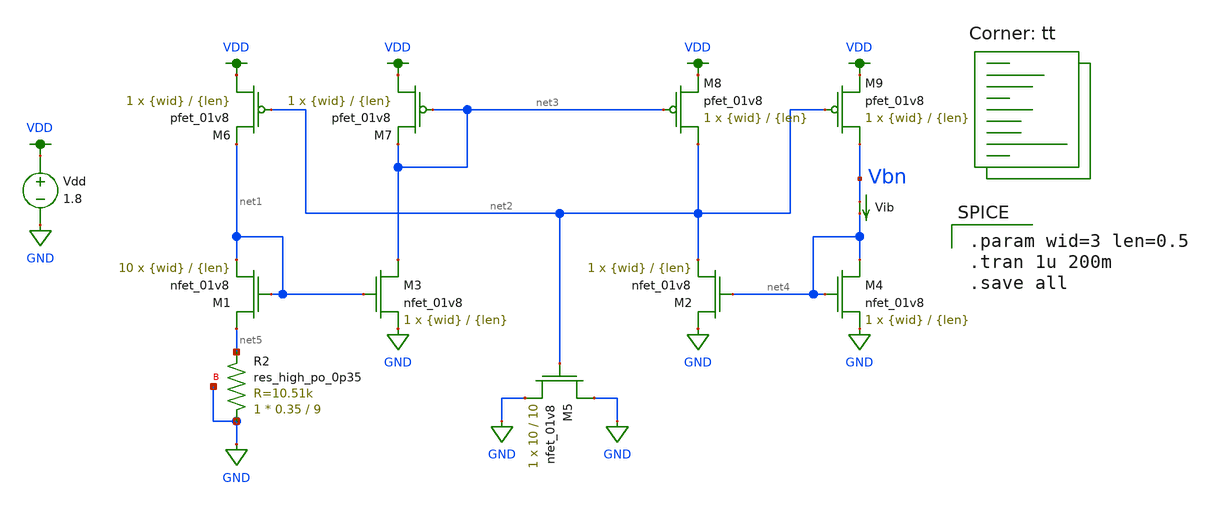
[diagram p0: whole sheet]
** sch_path: final/schematics/bias_gen/bias_gen_tb.sch
**.subckt bias_gen_tb
XM1 net5 net1 net1 GND sky130_fd_pr__nfet_01v8 L={len} W={wid} nf=1 ad='int((nf+1)/2) * W/nf * 0.29'
+ as='int((nf+2)/2) * W/nf * 0.29' pd='2*int((nf+1)/2) * (W/nf + 0.29)' ps='2*int((nf+2)/2) * (W/nf + 0.29)'
+ nrd='0.29 / W' nrs='0.29 / W' sa=0 sb=0 sd=0 mult=10 m=10
XM4 net4 net4 GND GND sky130_fd_pr__nfet_01v8 L={len} W={wid} nf=1 ad='int((nf+1)/2) * W/nf * 0.29' as='int((nf+2)/2) * W/nf * 0.29'
+ pd='2*int((nf+1)/2) * (W/nf + 0.29)' ps='2*int((nf+2)/2) * (W/nf + 0.29)' nrd='0.29 / W' nrs='0.29 / W'
+ sa=0 sb=0 sd=0 mult=1 m=1
XM5 GND net2 GND GND sky130_fd_pr__nfet_01v8 L=10 W=10 nf=1 ad='int((nf+1)/2) * W/nf * 0.29' as='int((nf+2)/2) * W/nf * 0.29'
+ pd='2*int((nf+1)/2) * (W/nf + 0.29)' ps='2*int((nf+2)/2) * (W/nf + 0.29)' nrd='0.29 / W' nrs='0.29 / W'
+ sa=0 sb=0 sd=0 mult=1 m=1
XM6 VDD net2 net1 VDD sky130_fd_pr__pfet_01v8 L={len} W={wid} nf=1 ad='int((nf+1)/2) * W/nf * 0.29' as='int((nf+2)/2) * W/nf * 0.29'
+ pd='2*int((nf+1)/2) * (W/nf + 0.29)' ps='2*int((nf+2)/2) * (W/nf + 0.29)' nrd='0.29 / W' nrs='0.29 / W'
+ sa=0 sb=0 sd=0 mult=1 m=1
XM2 GND net4 net2 GND sky130_fd_pr__nfet_01v8 L={len} W={wid} nf=1 ad='int((nf+1)/2) * W/nf * 0.29' as='int((nf+2)/2) * W/nf * 0.29'
+ pd='2*int((nf+1)/2) * (W/nf + 0.29)' ps='2*int((nf+2)/2) * (W/nf + 0.29)' nrd='0.29 / W' nrs='0.29 / W'
+ sa=0 sb=0 sd=0 mult=1 m=1
XM3 net3 net1 GND GND sky130_fd_pr__nfet_01v8 L={len} W={wid} nf=1 ad='int((nf+1)/2) * W/nf * 0.29' as='int((nf+2)/2) * W/nf * 0.29'
+ pd='2*int((nf+1)/2) * (W/nf + 0.29)' ps='2*int((nf+2)/2) * (W/nf + 0.29)' nrd='0.29 / W' nrs='0.29 / W'
+ sa=0 sb=0 sd=0 mult=1 m=1
XM7 VDD net3 net3 VDD sky130_fd_pr__pfet_01v8 L={len} W={wid} nf=1 ad='int((nf+1)/2) * W/nf * 0.29' as='int((nf+2)/2) * W/nf * 0.29'
+ pd='2*int((nf+1)/2) * (W/nf + 0.29)' ps='2*int((nf+2)/2) * (W/nf + 0.29)' nrd='0.29 / W' nrs='0.29 / W'
+ sa=0 sb=0 sd=0 mult=1 m=1
XM8 net2 net3 VDD VDD sky130_fd_pr__pfet_01v8 L={len} W={wid} nf=1 ad='int((nf+1)/2) * W/nf * 0.29' as='int((nf+2)/2) * W/nf * 0.29'
+ pd='2*int((nf+1)/2) * (W/nf + 0.29)' ps='2*int((nf+2)/2) * (W/nf + 0.29)' nrd='0.29 / W' nrs='0.29 / W'
+ sa=0 sb=0 sd=0 mult=1 m=1
XM9 Vbn net2 VDD VDD sky130_fd_pr__pfet_01v8 L={len} W={wid} nf=1 ad='int((nf+1)/2) * W/nf * 0.29' as='int((nf+2)/2) * W/nf * 0.29'
+ pd='2*int((nf+1)/2) * (W/nf + 0.29)' ps='2*int((nf+2)/2) * (W/nf + 0.29)' nrd='0.29 / W' nrs='0.29 / W'
+ sa=0 sb=0 sd=0 mult=1 m=1
Vdd VDD GND 1.8
Vib Vbn net4 0
.save i(vib)
XR2 GND net5 GND sky130_fd_pr__res_high_po_0p35 L=9 mult=1 m=1
**** begin user architecture code

.param wid=3 len=0.5
.tran 1u 200m
.save all


.lib $::SKYWATER_MODELS/sky130.lib.spice tt
**** end user architecture code
**.ends
.GLOBAL VDD
.GLOBAL GND
.end
